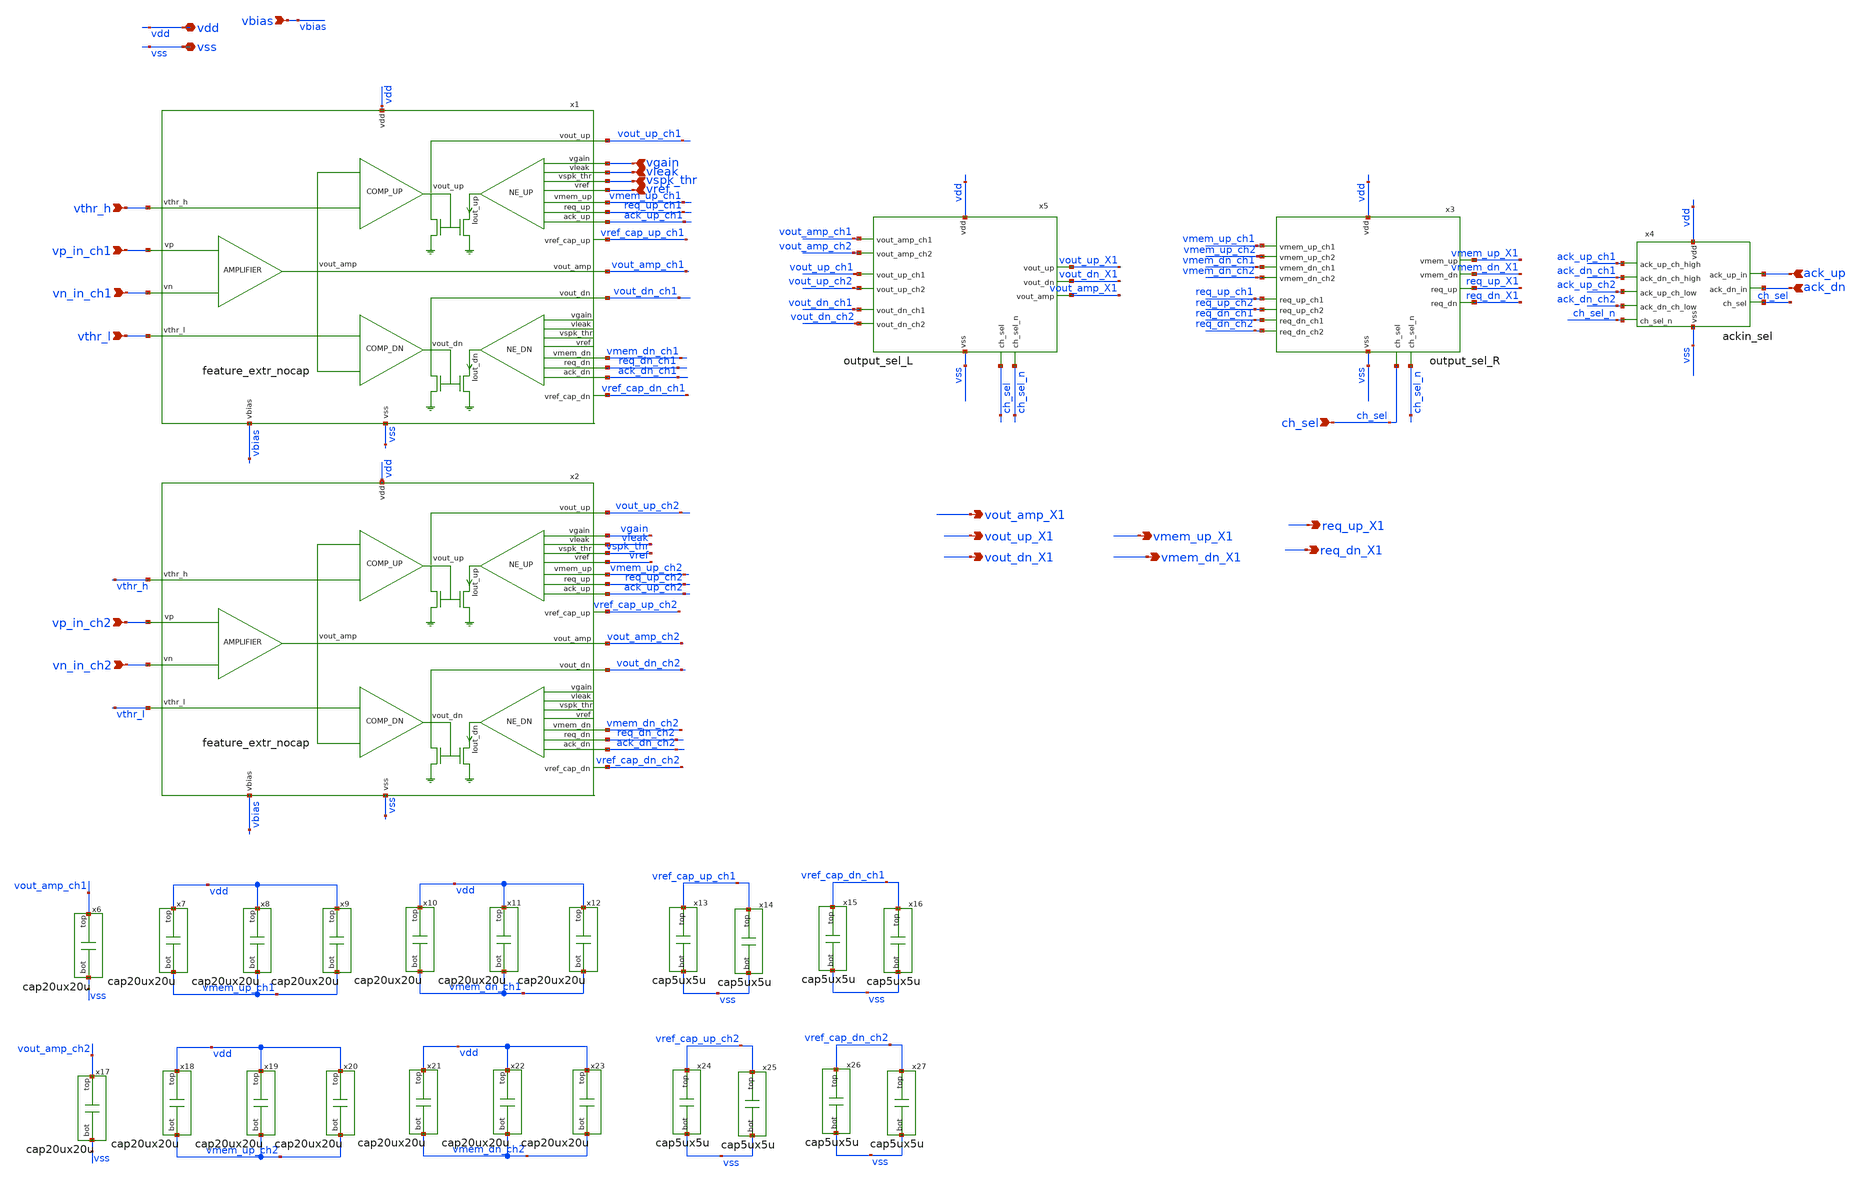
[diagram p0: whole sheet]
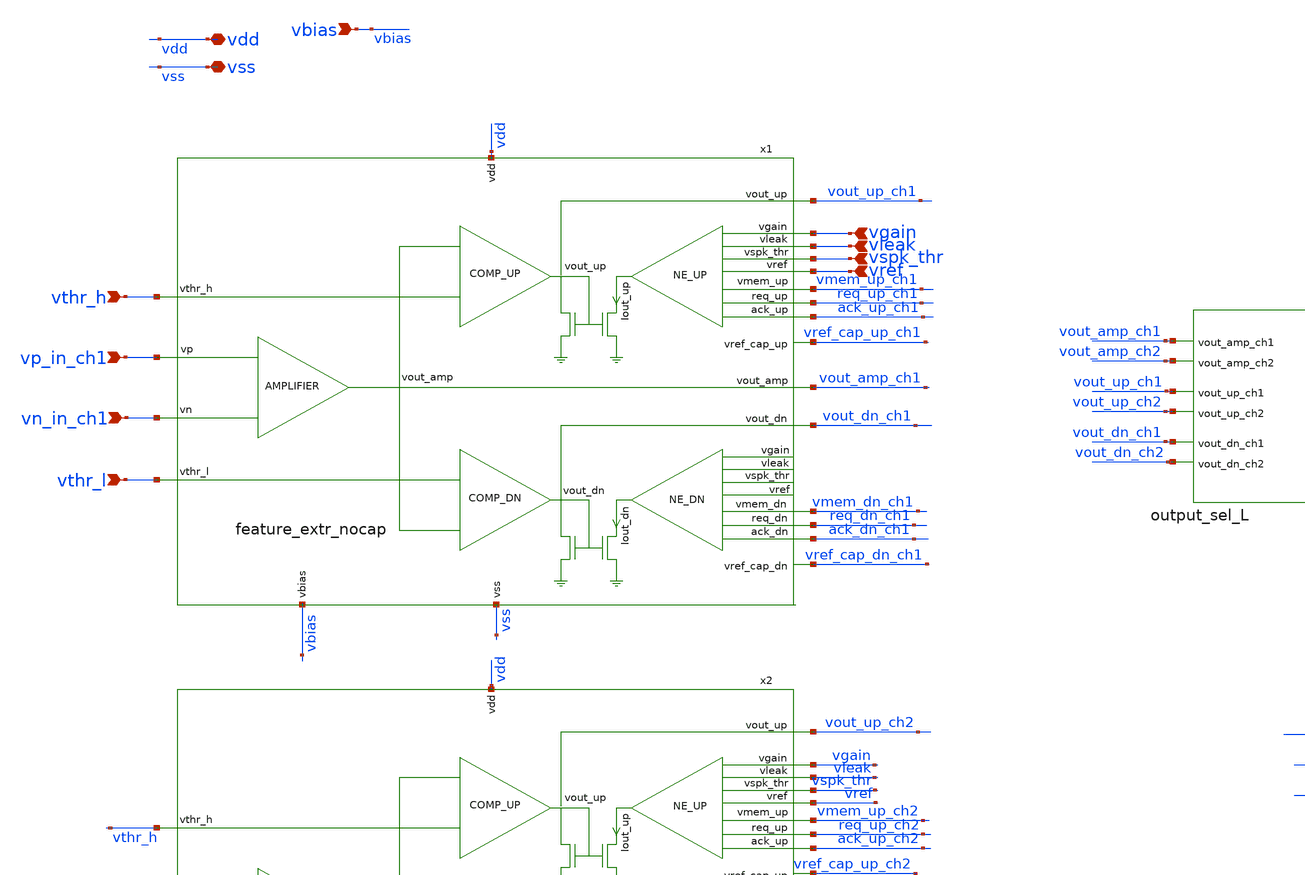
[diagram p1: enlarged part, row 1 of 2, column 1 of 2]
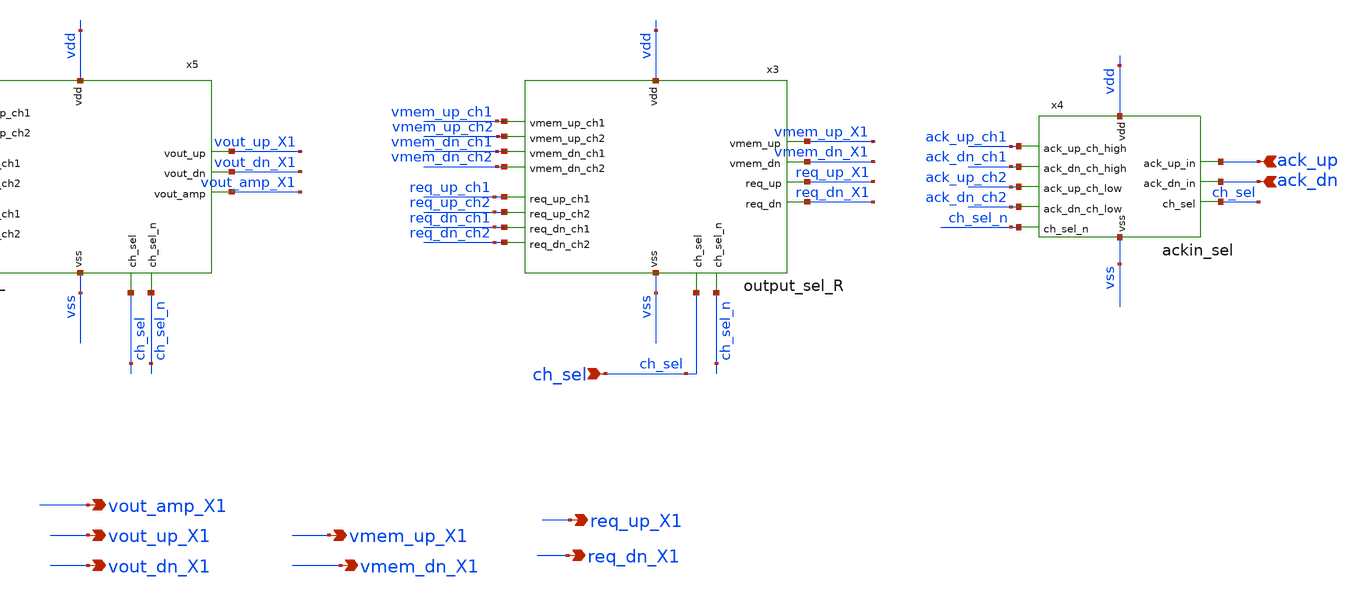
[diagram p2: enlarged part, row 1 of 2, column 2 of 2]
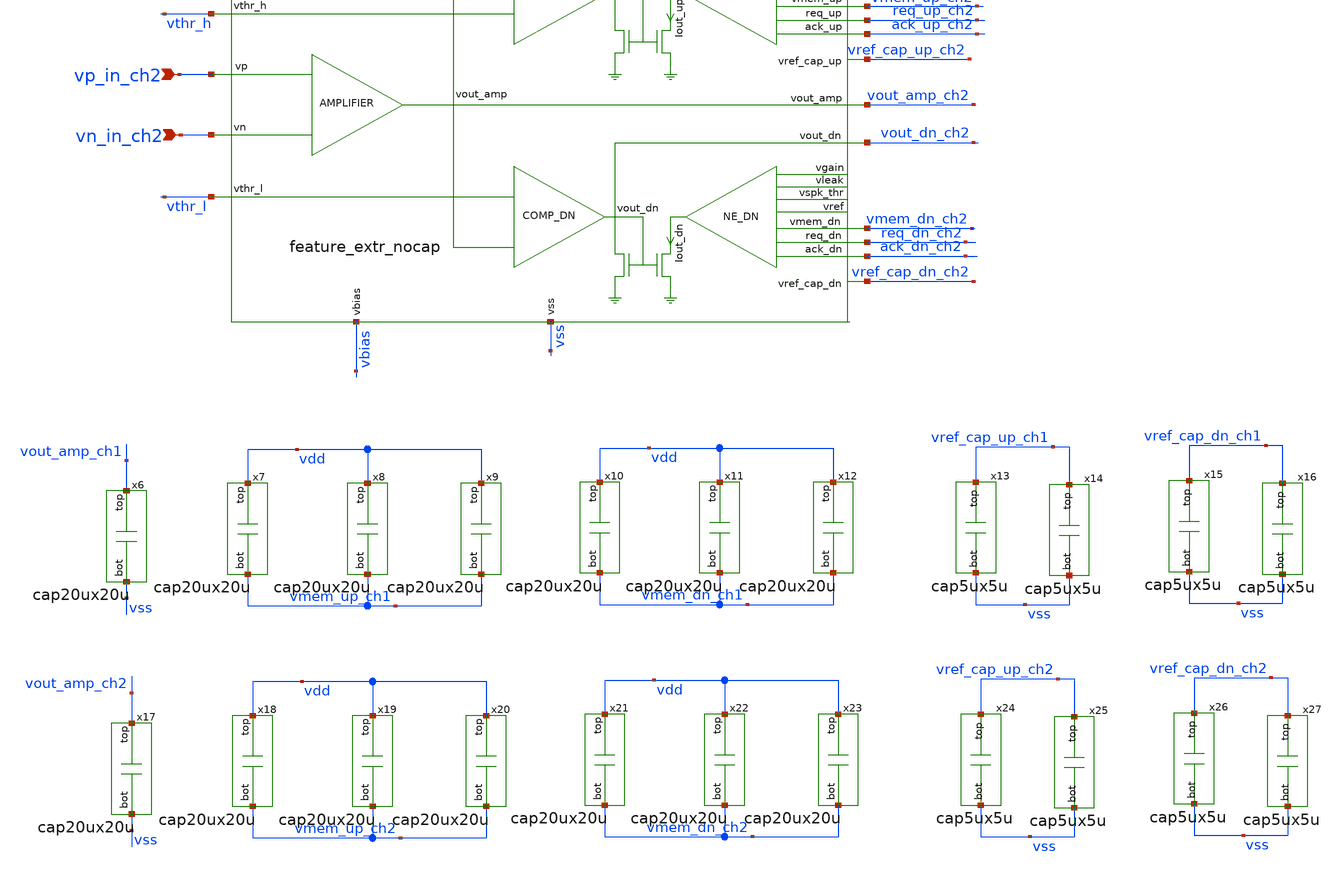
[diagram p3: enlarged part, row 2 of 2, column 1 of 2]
** sch_path: v2_feature_extr/2ch_feature_extr_wobuf.sch
**.subckt 2ch_feature_extr_wobuf vdd vss vbias vthr_h vthr_l vgain vleak vspk_thr vref vp_in_ch1
*+ vn_in_ch1 vp_in_ch2 vn_in_ch2 vout_amp_X1 vout_up_X1 vout_dn_X1 vmem_up_X1 vmem_dn_X1 req_up_X1 req_dn_X1
*+ ack_up ack_dn ch_sel
*.iopin vdd
*.iopin vss
*.ipin vbias
*.ipin vthr_h
*.ipin vthr_l
*.ipin vgain
*.ipin vleak
*.ipin vspk_thr
*.ipin vref
*.ipin vp_in_ch1
*.ipin vn_in_ch1
*.ipin vp_in_ch2
*.ipin vn_in_ch2
*.opin vout_amp_X1
*.opin vout_up_X1
*.opin vout_dn_X1
*.opin vmem_up_X1
*.opin vmem_dn_X1
*.opin req_up_X1
*.opin req_dn_X1
*.ipin ack_up
*.ipin ack_dn
*.ipin ch_sel
x1 vref_cap_up_ch1 vout_up_ch1 vleak vspk_thr vref vdd vmem_up_ch1 vthr_h req_up_ch1 vss ack_up_ch1
+ vbias vp_in_ch1 vout_amp_ch1 vn_in_ch1 vout_dn_ch1 vthr_l vmem_dn_ch1 req_dn_ch1 ack_dn_ch1 vgain
+ vref_cap_dn_ch1 feature_extr_nocap
x2 vref_cap_up_ch2 vout_up_ch2 vleak vspk_thr vref vdd vmem_up_ch2 vthr_h req_up_ch2 vss ack_up_ch2
+ vbias vp_in_ch2 vout_amp_ch2 vn_in_ch2 vout_dn_ch2 vthr_l vmem_dn_ch2 req_dn_ch2 ack_dn_ch2 vgain
+ vref_cap_dn_ch2 feature_extr_nocap
x3 vdd vss ch_sel vmem_up_ch2 vmem_dn_ch2 req_dn_ch2 req_up_ch2 vmem_up_X1 vmem_dn_X1 req_dn_X1
+ req_up_X1 vmem_up_ch1 vmem_dn_ch1 req_dn_ch1 req_up_ch1 ch_sel_n output_sel_R
x4 ack_up vdd vss ack_dn ch_sel ack_up_ch1 ack_dn_ch1 ack_up_ch2 ack_dn_ch2 ch_sel_n ackin_sel
x5 vdd vss vout_dn_ch2 vout_up_ch2 vout_amp_ch2 vout_dn_X1 ch_sel_n vout_up_X1 vout_amp_X1
+ vout_dn_ch1 vout_up_ch1 vout_amp_ch1 ch_sel output_sel_L
x6 vout_amp_ch1 vss cap20ux20u
x7 vdd vmem_up_ch1 cap20ux20u
x8 vdd vmem_up_ch1 cap20ux20u
x9 vdd vmem_up_ch1 cap20ux20u
x10 vdd vmem_dn_ch1 cap20ux20u
x11 vdd vmem_dn_ch1 cap20ux20u
x12 vdd vmem_dn_ch1 cap20ux20u
x13 vref_cap_up_ch1 vss cap5ux5u
x14 vref_cap_up_ch1 vss cap5ux5u
x15 vref_cap_dn_ch1 vss cap5ux5u
x16 vref_cap_dn_ch1 vss cap5ux5u
x17 vout_amp_ch2 vss cap20ux20u
x18 vdd vmem_up_ch2 cap20ux20u
x19 vdd vmem_up_ch2 cap20ux20u
x20 vdd vmem_up_ch2 cap20ux20u
x21 vdd vmem_dn_ch2 cap20ux20u
x22 vdd vmem_dn_ch2 cap20ux20u
x23 vdd vmem_dn_ch2 cap20ux20u
x24 vref_cap_up_ch2 vss cap5ux5u
x25 vref_cap_up_ch2 vss cap5ux5u
x26 vref_cap_dn_ch2 vss cap5ux5u
x27 vref_cap_dn_ch2 vss cap5ux5u
**.ends
.end
